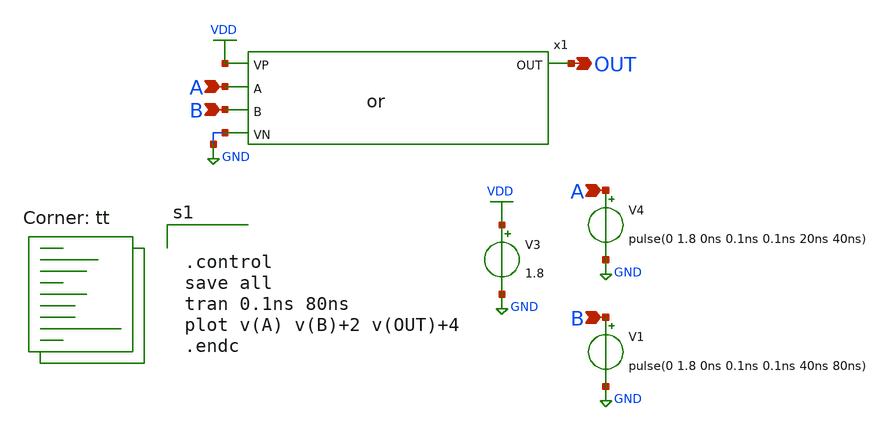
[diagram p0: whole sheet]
** sch_path: dff/xschem/tb_xschem_dff.sch
**.subckt tb_xschem_dff A B A B OUT
*.ipin A
*.ipin B
*.ipin A
*.ipin B
*.opin OUT
V3 VDD GND 1.8
V4 A GND pulse(0 1.8 0ns 0.1ns 0.1ns 20ns 40ns)
V1 B GND pulse(0 1.8 0ns 0.1ns 0.1ns 40ns 80ns)
x1 VDD OUT A B GND or
**** begin user architecture code
.lib $::SKYWATER_MODELS/sky130.lib.spice tt


.control
save all
tran 0.1ns 80ns
plot v(A) v(B)+2 v(OUT)+4
.endc


**** end user architecture code
**.ends

* expanding   symbol:  or.sym # of pins=5
** sym_path: basic_cell/or/xschem/or.sym
** sch_path: basic_cell/or/xschem/or.sch
.subckt or VP OUT A B VN
*.ipin VP
*.ipin A
*.ipin B
*.ipin VN
*.opin OUT
x1 VP A B net1 VN nor
x2 VP net1 OUT VN inverter
.ends


* expanding   symbol:  /foss/designs/APIC_Mux_DFF/basic_cell/single_cell/nor/nor.sym # of pins=5
** sym_path: basic_cell/single_cell/nor/nor.sym
** sch_path: basic_cell/single_cell/nor/nor.sch
.subckt nor VP A B OUT VN
*.ipin A
*.ipin B
*.ipin VP
*.ipin VN
*.opin OUT
XM1 OUT A VN VN sky130_fd_pr__nfet_01v8 L=0.15 W=1 nf=1 ad='int((nf+1)/2) * W/nf * 0.29' as='int((nf+2)/2) * W/nf * 0.29'
+ pd='2*int((nf+1)/2) * (W/nf + 0.29)' ps='2*int((nf+2)/2) * (W/nf + 0.29)' nrd='0.29 / W' nrs='0.29 / W'
+ sa=0 sb=0 sd=0 mult=1 m=1
XM2 OUT B VN VN sky130_fd_pr__nfet_01v8 L=0.15 W=1 nf=1 ad='int((nf+1)/2) * W/nf * 0.29' as='int((nf+2)/2) * W/nf * 0.29'
+ pd='2*int((nf+1)/2) * (W/nf + 0.29)' ps='2*int((nf+2)/2) * (W/nf + 0.29)' nrd='0.29 / W' nrs='0.29 / W'
+ sa=0 sb=0 sd=0 mult=1 m=1
XM3 OUT B net1 VP sky130_fd_pr__pfet_01v8 L=0.15 W=3 nf=1 ad='int((nf+1)/2) * W/nf * 0.29' as='int((nf+2)/2) * W/nf * 0.29'
+ pd='2*int((nf+1)/2) * (W/nf + 0.29)' ps='2*int((nf+2)/2) * (W/nf + 0.29)' nrd='0.29 / W' nrs='0.29 / W'
+ sa=0 sb=0 sd=0 mult=1 m=1
XM4 net1 A VP VP sky130_fd_pr__pfet_01v8 L=0.15 W=3 nf=1 ad='int((nf+1)/2) * W/nf * 0.29' as='int((nf+2)/2) * W/nf * 0.29'
+ pd='2*int((nf+1)/2) * (W/nf + 0.29)' ps='2*int((nf+2)/2) * (W/nf + 0.29)' nrd='0.29 / W' nrs='0.29 / W'
+ sa=0 sb=0 sd=0 mult=1 m=1
.ends


* expanding   symbol:  /foss/designs/APIC_Mux_DFF/basic_cell/single_cell/inverter/inverter.sym # of
*+ pins=4
** sym_path: basic_cell/single_cell/inverter/inverter.sym
** sch_path: basic_cell/single_cell/inverter/inverter.sch
.subckt inverter VP A OUT VN
*.ipin A
*.ipin VP
*.ipin VN
*.opin OUT
XM1 OUT A VP VP sky130_fd_pr__pfet_01v8 L=0.15 W=3 nf=1 ad='int((nf+1)/2) * W/nf * 0.29' as='int((nf+2)/2) * W/nf * 0.29'
+ pd='2*int((nf+1)/2) * (W/nf + 0.29)' ps='2*int((nf+2)/2) * (W/nf + 0.29)' nrd='0.29 / W' nrs='0.29 / W'
+ sa=0 sb=0 sd=0 mult=1 m=1
XM2 OUT A VN VN sky130_fd_pr__nfet_01v8 L=0.15 W=1 nf=1 ad='int((nf+1)/2) * W/nf * 0.29' as='int((nf+2)/2) * W/nf * 0.29'
+ pd='2*int((nf+1)/2) * (W/nf + 0.29)' ps='2*int((nf+2)/2) * (W/nf + 0.29)' nrd='0.29 / W' nrs='0.29 / W'
+ sa=0 sb=0 sd=0 mult=1 m=1
.ends

.GLOBAL VDD
.GLOBAL GND
.end
